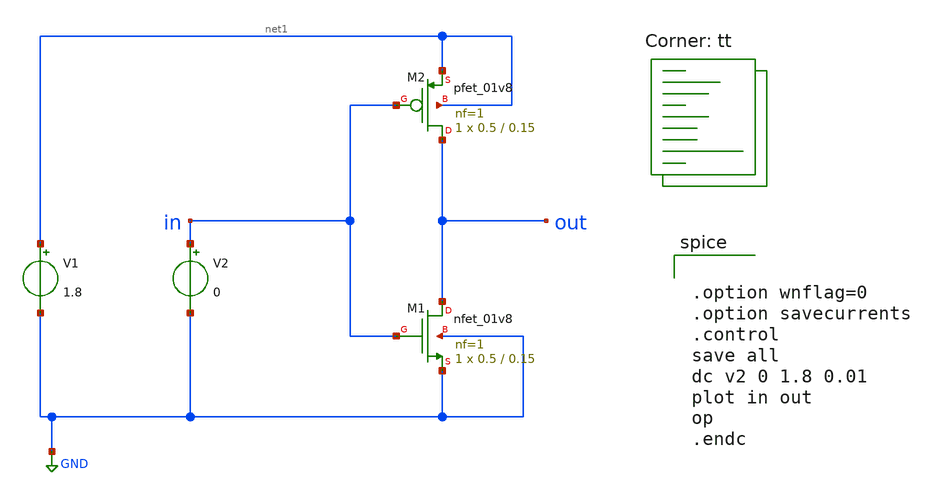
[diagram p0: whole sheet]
** sch_path: inverter.sch
**.subckt inverter
V1 net1 GND 1.8
V2 in GND 0
XM1 out in GND GND sky130_fd_pr__nfet_01v8 L=0.15 W=0.5 nf=1 ad='int((nf+1)/2) * W/nf * 0.29' as='int((nf+2)/2) * W/nf * 0.29'
+ pd='2*int((nf+1)/2) * (W/nf + 0.29)' ps='2*int((nf+2)/2) * (W/nf + 0.29)' nrd='0.29 / W' nrs='0.29 / W'
+ sa=0 sb=0 sd=0 mult=1 m=1
XM2 out in net1 net1 sky130_fd_pr__pfet_01v8 L=0.15 W=0.5 nf=1 ad='int((nf+1)/2) * W/nf * 0.29' as='int((nf+2)/2) * W/nf * 0.29'
+ pd='2*int((nf+1)/2) * (W/nf + 0.29)' ps='2*int((nf+2)/2) * (W/nf + 0.29)' nrd='0.29 / W' nrs='0.29 / W'
+ sa=0 sb=0 sd=0 mult=1 m=1
**** begin user architecture code


.option wnflag=0
.option savecurrents
.control
save all
dc v2 0 1.8 0.01
plot in out
op
.endc


.lib $::SKYWATER_MODELS/sky130.lib.spice tt
**** end user architecture code
**.ends
.GLOBAL GND
.end
